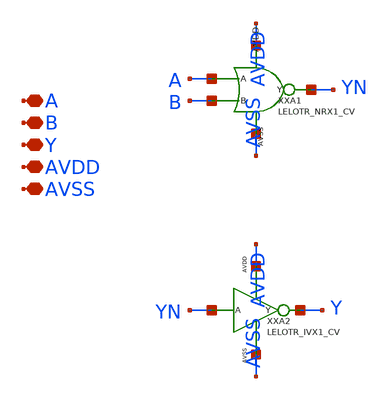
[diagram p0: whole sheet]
** sch_path: design/LELO_TR_GF180MCUD/LELOTR_ORX1_CV.sch
**.subckt LELOTR_ORX1_CV A B Y AVDD AVSS
*.iopin A
*.iopin B
*.iopin Y
*.iopin AVDD
*.iopin AVSS
XXA1 A B YN AVDD AVSS LELOTR_NRX1_CV
XXA2 YN Y AVDD AVSS LELOTR_IVX1_CV
**.ends
.end
